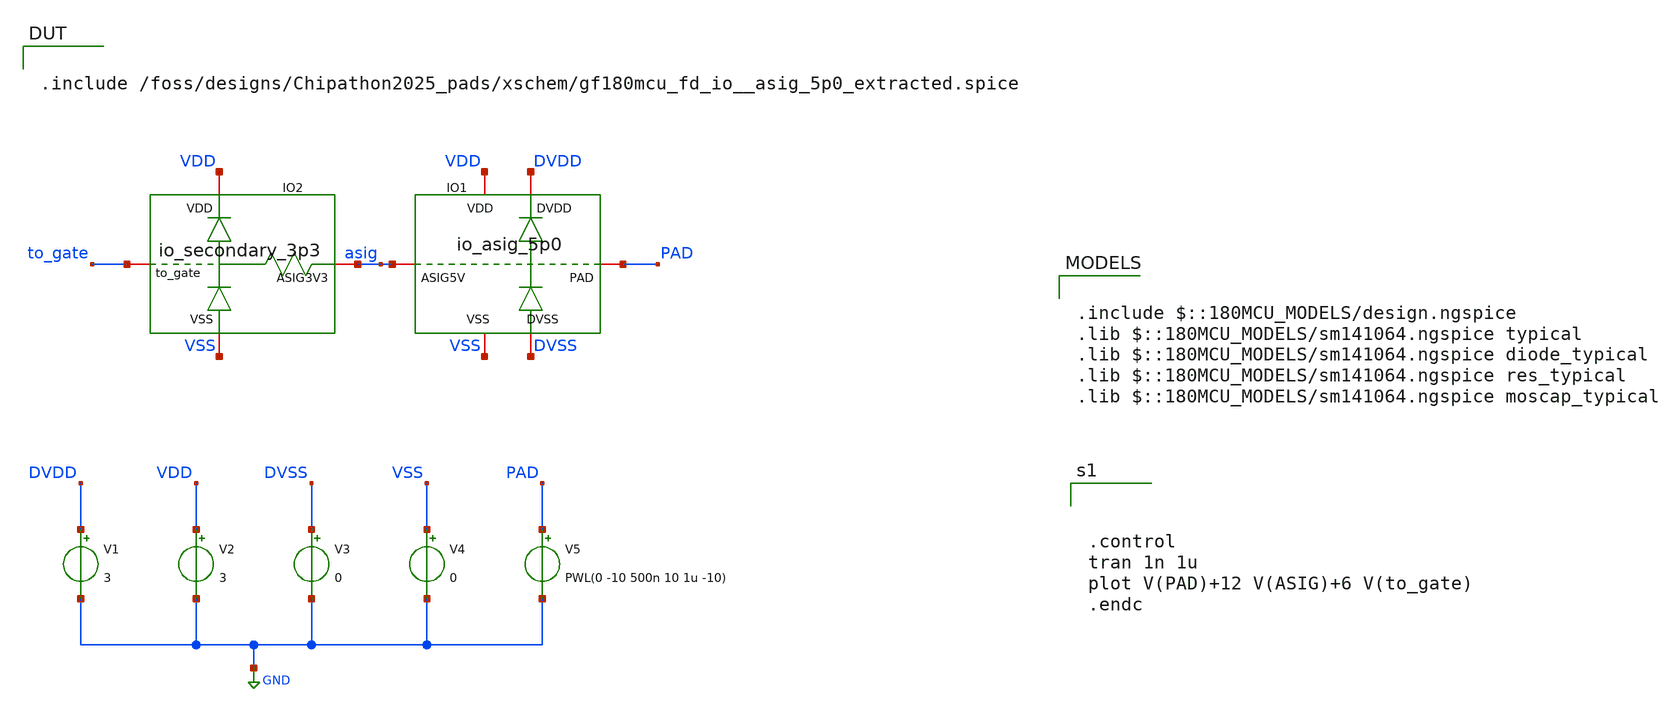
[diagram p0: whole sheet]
** sch_path: examples/pads_simulation/io_secondary_3p3_DC_tb.sch
**.subckt io_secondary_3p3_DC_tb
V1 DVDD GND 3
V2 VDD GND 3
V3 DVSS GND 0
V4 VSS GND 0
V5 PAD GND PWL(0 -10 500n 10 1u -10)
XIO1 DVSS DVDD VSS VDD PAD asig gf180mcu_fd_io__asig_5p0_extracted
XIO2 VDD to_gate asig VSS io_secondary_3p3
**** begin user architecture code

.include /foss/designs/Chipathon2025_pads/xschem/gf180mcu_fd_io__asig_5p0_extracted.spice


.include $::180MCU_MODELS/design.ngspice
.lib $::180MCU_MODELS/sm141064.ngspice typical
.lib $::180MCU_MODELS/sm141064.ngspice diode_typical
.lib $::180MCU_MODELS/sm141064.ngspice res_typical
.lib $::180MCU_MODELS/sm141064.ngspice moscap_typical




.control
tran 1n 1u
plot V(PAD)+12 V(ASIG)+6 V(to_gate)
.endc


**** end user architecture code
**.ends

* expanding   symbol:  Chipathon2025_pads/xschem/symbols/io_secondary_3p3/io_secondary_3p3.sym # of
*+ pins=4
** sym_path: resources/Integration/Chipathon2025_pads/xschem/symbols/io_secondary_3p3/io_secondary_3p3.sym
** sch_path: resources/Integration/Chipathon2025_pads/xschem/symbols/io_secondary_3p3/io_secondary_3p3.sch
.subckt io_secondary_3p3 VDD to_gate ASIG3V3 VSS


*.iopin VSS
*.iopin VDD
*.iopin to_gate
*.iopin ASIG3V3
XR1 to_gate ASIG3V3 VDD ppolyf_u r_width=16e-6 r_length=4e-6 m=1
D2 VSS to_gate diode_nd2ps_03v3 area='10u * 10u ' pj='2*10u + 2*10u ' m=4
D1 to_gate VDD diode_pd2nw_03v3 area='10u * 10u ' pj='2*10u + 2*10u ' m=4
.ends

.GLOBAL GND
.end
